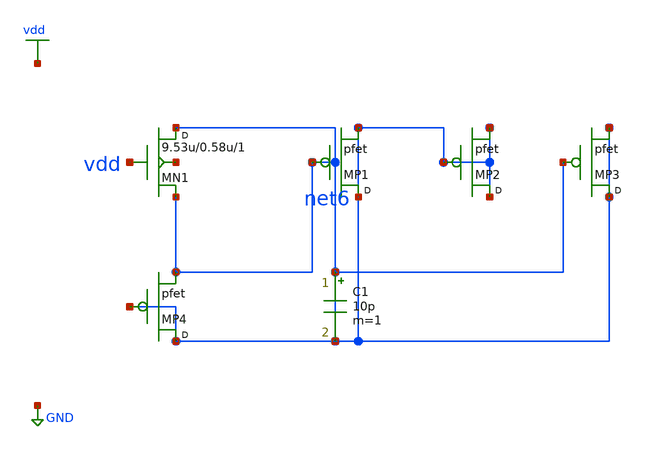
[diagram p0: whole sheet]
** sch_path: synthetic/generated/0031_synthetic.sch
**.subckt 0031_synthetic
MN1 net6 vdd net6 net1 nfet w=9.53u l=0.58u m=1
MP1 net6 net6 net6 pfet m=1
MP2 net6 net6 net6 pfet m=1
MP3 net6 net6 net6 pfet m=1
MP4 net6 net6 net6 pfet m=1
C1 net6 net6 10p m=1
**.ends
.GLOBAL vdd
.GLOBAL GND
.end
